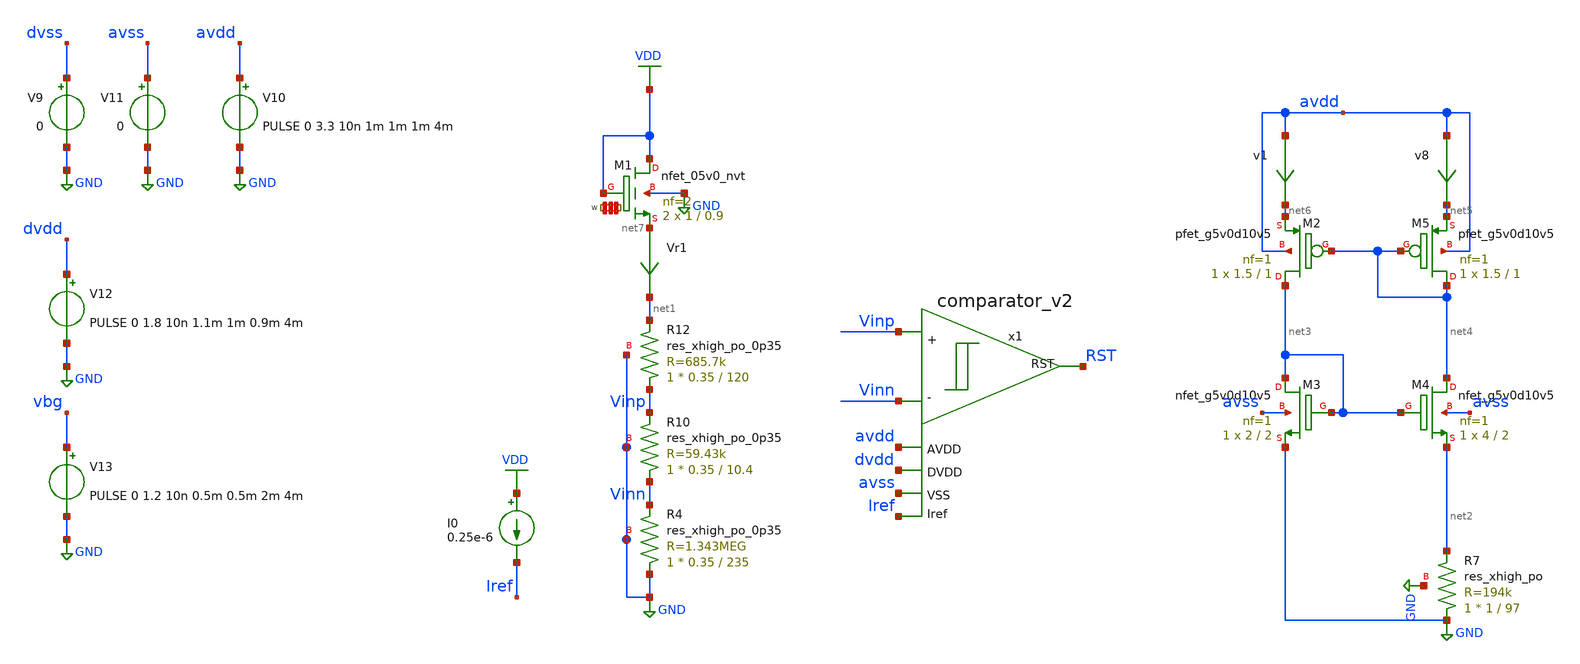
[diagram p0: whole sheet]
** sch_path: xschem_sim/comparator_tb.sch
**.subckt comparator_tb
x1 Iref Vinn Vinp RST avss avdd dvdd comparator_v2
v8 avdd net5 0
.save i(v8)
V9 dvss GND 0
V10 avdd GND PULSE 0 3.3 10n 1m 1m 1m 4m
V11 avss GND 0
V12 dvdd GND PULSE 0 1.8 10n 1.1m 1m 0.9m 4m
V13 vbg GND PULSE 0 1.2 10n 0.5m 0.5m 2m 4m
XM1 VDD VDD net7 GND sky130_fd_pr__nfet_05v0_nvt L=0.9 W='1 * 2 ' nf=2 ad='int((nf+1)/2) * W / nf * 0.29'
+ as='int((nf+2)/2) * W / nf * 0.29' pd='2*int((nf+1)/2) * (W / nf + 0.29)' ps='2*int((nf+2)/2) * (W / nf + 0.29)'
+ nrd='0.29 / W ' nrs='0.29 / W ' sa=0 sb=0 sd=0 mult=2 m=2
Vr1 net7 net1 0
.save i(vr1)
XR4 GND Vinn GND sky130_fd_pr__res_xhigh_po_0p35 L=235 mult=1 m=1
XR10 Vinn Vinp GND sky130_fd_pr__res_xhigh_po_0p35 L=10.4 mult=1 m=1
XR12 Vinp net1 GND sky130_fd_pr__res_xhigh_po_0p35 L=120 mult=1 m=1
I0 VDD Iref 0.25e-6
XM2 net3 net4 net6 avdd sky130_fd_pr__pfet_g5v0d10v5 L=1 W=1.5 nf=1 ad='int((nf+1)/2) * W/nf * 0.29'
+ as='int((nf+2)/2) * W/nf * 0.29' pd='2*int((nf+1)/2) * (W/nf + 0.29)' ps='2*int((nf+2)/2) * (W/nf + 0.29)'
+ nrd='0.29 / W' nrs='0.29 / W' sa=0 sb=0 sd=0 mult=1 m=1
XM3 net3 net3 GND avss sky130_fd_pr__nfet_g5v0d10v5 L=2 W=2 nf=1 ad='int((nf+1)/2) * W/nf * 0.29' as='int((nf+2)/2) * W/nf * 0.29'
+ pd='2*int((nf+1)/2) * (W/nf + 0.29)' ps='2*int((nf+2)/2) * (W/nf + 0.29)' nrd='0.29 / W' nrs='0.29 / W'
+ sa=0 sb=0 sd=0 mult=1 m=1
XM4 net4 net3 net2 avss sky130_fd_pr__nfet_g5v0d10v5 L=2 W=4 nf=1 ad='int((nf+1)/2) * W/nf * 0.29' as='int((nf+2)/2) * W/nf * 0.29'
+ pd='2*int((nf+1)/2) * (W/nf + 0.29)' ps='2*int((nf+2)/2) * (W/nf + 0.29)' nrd='0.29 / W' nrs='0.29 / W'
+ sa=0 sb=0 sd=0 mult=1 m=1
XR7 GND net2 GND sky130_fd_pr__res_xhigh_po W=1 L=97 mult=1 m=1
XM5 net4 net4 net5 avdd sky130_fd_pr__pfet_g5v0d10v5 L=1 W=1.5 nf=1 ad='int((nf+1)/2) * W/nf * 0.29'
+ as='int((nf+2)/2) * W/nf * 0.29' pd='2*int((nf+1)/2) * (W/nf + 0.29)' ps='2*int((nf+2)/2) * (W/nf + 0.29)'
+ nrd='0.29 / W' nrs='0.29 / W' sa=0 sb=0 sd=0 mult=1 m=1
v1 avdd net6 0
.save i(v1)
**** begin user architecture code
 .lib $::SKYWATER_MODELS/sky130.lib.spice tt

.include $::SKYWATER_STDCELLS/sky130_fd_sc_hd.spice
.include $::SKYWATER_STDCELLS/../../sky130_fd_sc_hvl/spice/sky130_fd_sc_hvl.spice




*.option method=gear
.options savecurrents
.control
set temp=27
save all
tran 1u 8m
plot AVDD RST
meas tran Ivdd AVG i(V10)
write comparator_tb.raw
*quit 0
.endc


**** end user architecture code
**.ends
.GLOBAL GND
.GLOBAL VDD
.end
